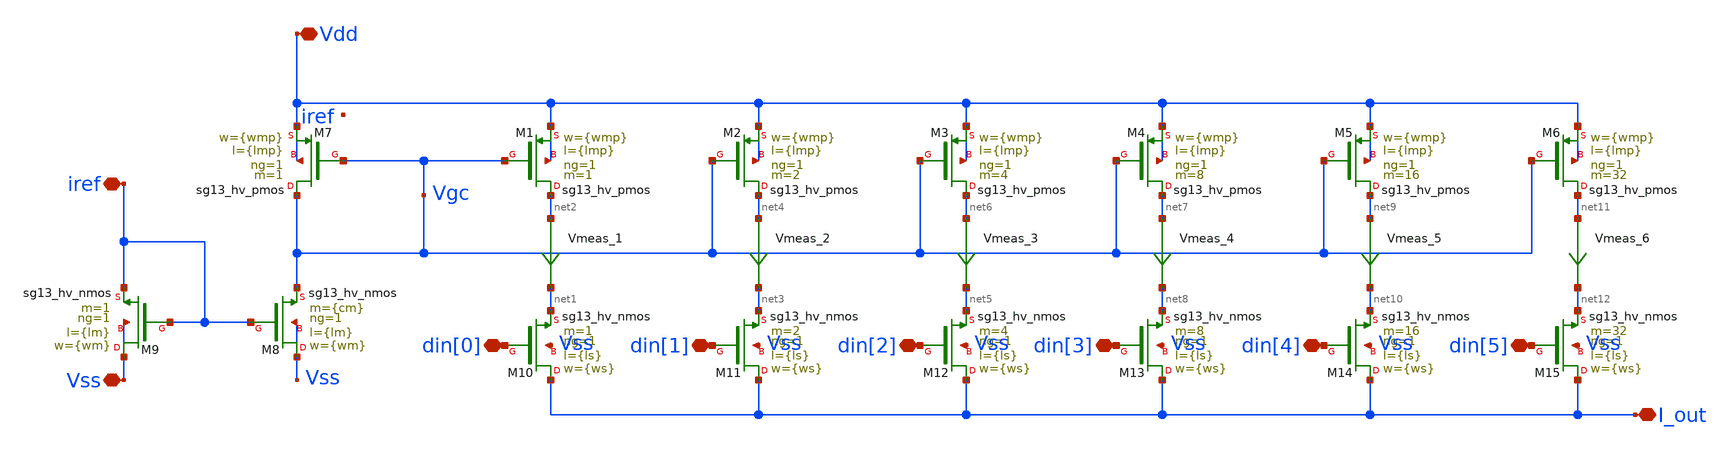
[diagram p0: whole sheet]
** sch_path: 6b_Current_DAC/design_data/xschem/idac.sch
**.subckt idac I_out Vss iref Vdd din[0] din[1] din[2] din[3] din[4] din[5]
*.iopin I_out
*.iopin Vss
*.iopin iref
*.iopin Vdd
*.iopin din[0]
*.iopin din[1]
*.iopin din[2]
*.iopin din[3]
*.iopin din[4]
*.iopin din[5]
XM8 Vss iref Vgc Vss sg13_hv_nmos w={wm} l={lm} ng=1 m={cm} mm_ok=1
XM9 Vss iref iref Vss sg13_hv_nmos w={wm} l={lm} ng=1 m=1 mm_ok=1
XM10 I_out din[0] net1 Vss sg13_hv_nmos w={ws} l={ls} ng=1 m=1 mm_ok=1
XM11 I_out din[1] net3 Vss sg13_hv_nmos w={ws} l={ls} ng=1 m=2 mm_ok=1
XM12 I_out din[2] net5 Vss sg13_hv_nmos w={ws} l={ls} ng=1 m=4 mm_ok=1
XM13 I_out din[3] net8 Vss sg13_hv_nmos w={ws} l={ls} ng=1 m=8 mm_ok=1
XM14 I_out din[4] net10 Vss sg13_hv_nmos w={ws} l={ls} ng=1 m=16 mm_ok=1
XM15 I_out din[5] net12 Vss sg13_hv_nmos w={ws} l={ls} ng=1 m=32 mm_ok=1
Vmeas_1 net2 net1 0
.save i(vmeas_1)
Vmeas_2 net4 net3 0
.save i(vmeas_2)
Vmeas_3 net6 net5 0
.save i(vmeas_3)
Vmeas_4 net7 net8 0
.save i(vmeas_4)
Vmeas_5 net9 net10 0
.save i(vmeas_5)
Vmeas_6 net11 net12 0
.save i(vmeas_6)
XM1 net2 Vgc Vdd Vdd sg13_hv_pmos w={wmp} l={lmp} ng=1 m=1 mm_ok=1
XM7 Vgc Vgc Vdd Vdd sg13_hv_pmos w={wmp} l={lmp} ng=1 m=1 mm_ok=1
XM2 net4 Vgc Vdd Vdd sg13_hv_pmos w={wmp} l={lmp} ng=1 m=2 mm_ok=1
XM3 net6 Vgc Vdd Vdd sg13_hv_pmos w={wmp} l={lmp} ng=1 m=4 mm_ok=1
XM4 net7 Vgc Vdd Vdd sg13_hv_pmos w={wmp} l={lmp} ng=1 m=8 mm_ok=1
XM5 net9 Vgc Vdd Vdd sg13_hv_pmos w={wmp} l={lmp} ng=1 m=16 mm_ok=1
XM6 net11 Vgc Vdd Vdd sg13_hv_pmos w={wmp} l={lmp} ng=1 m=32 mm_ok=1
**.ends
.end
